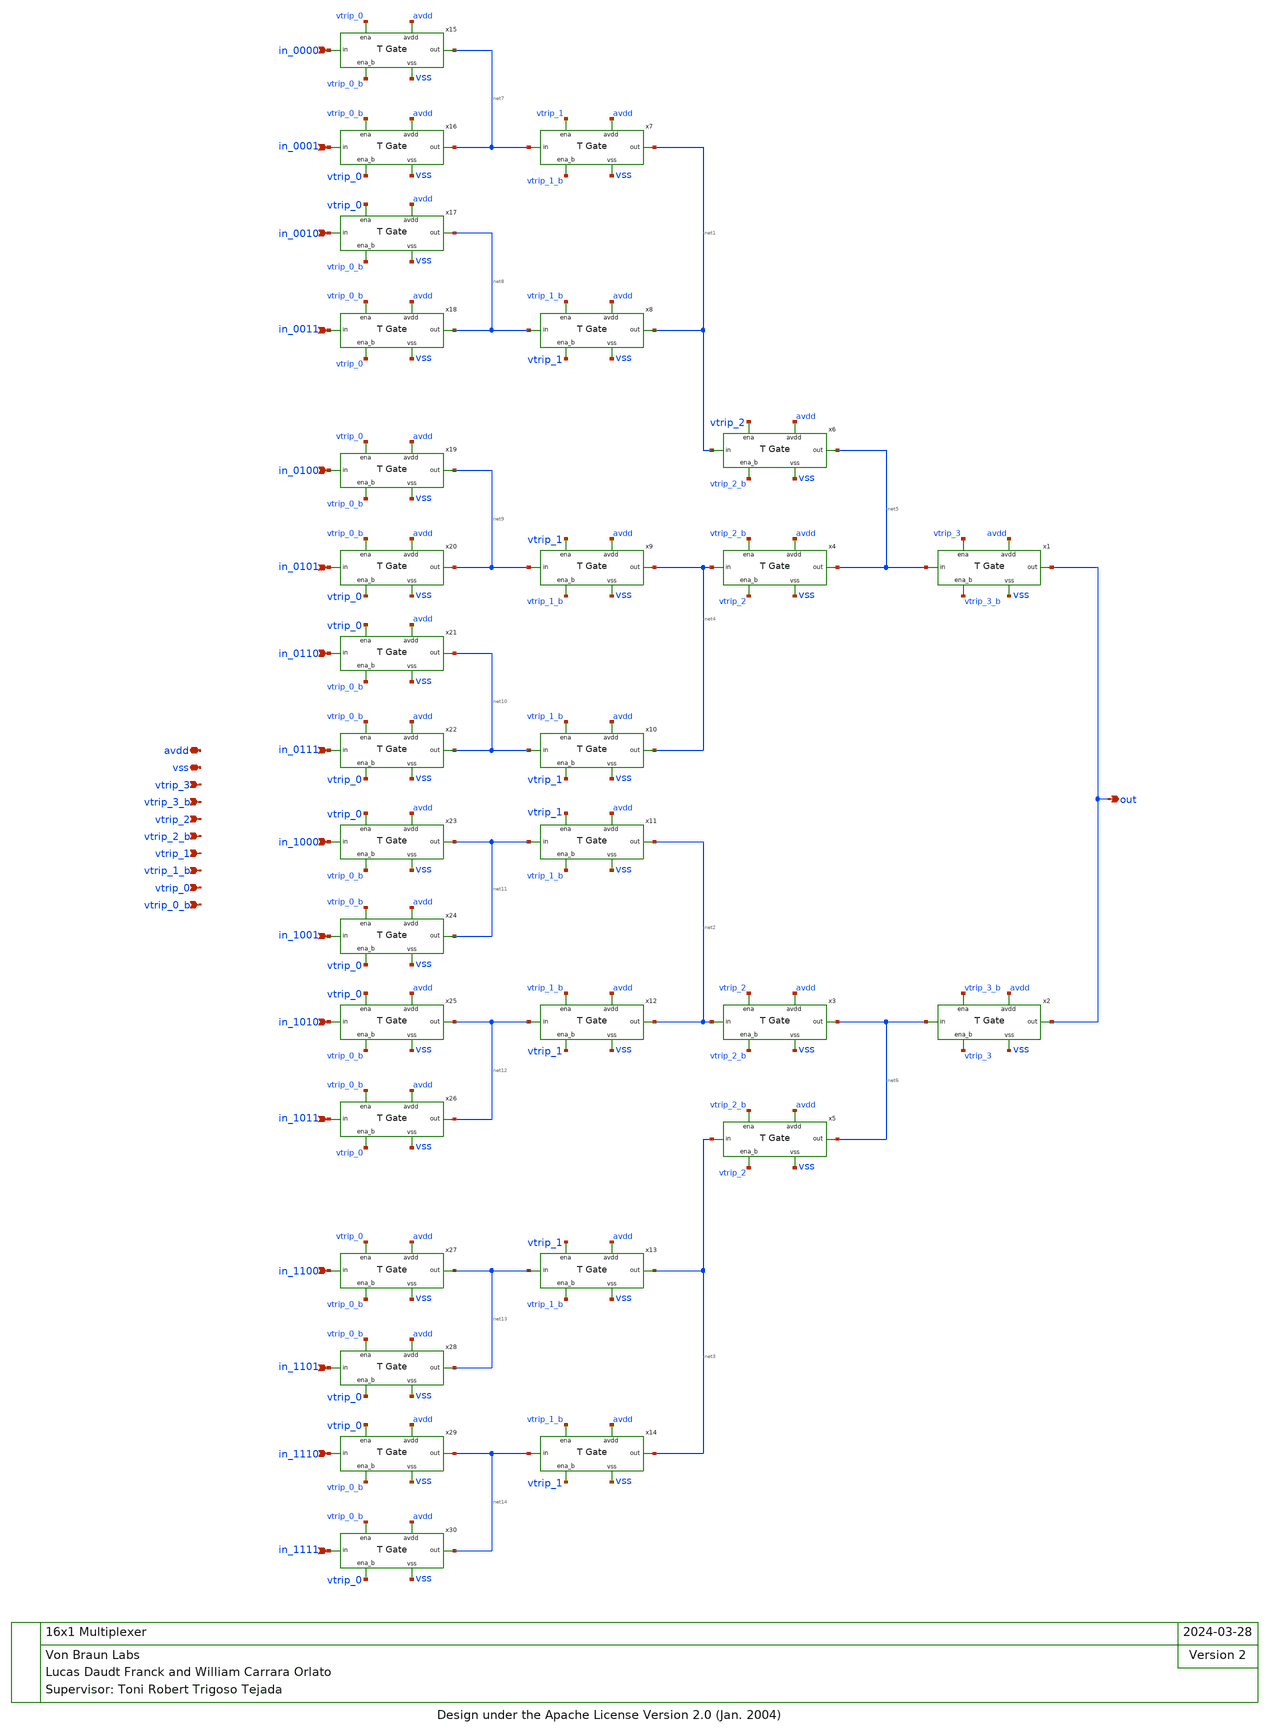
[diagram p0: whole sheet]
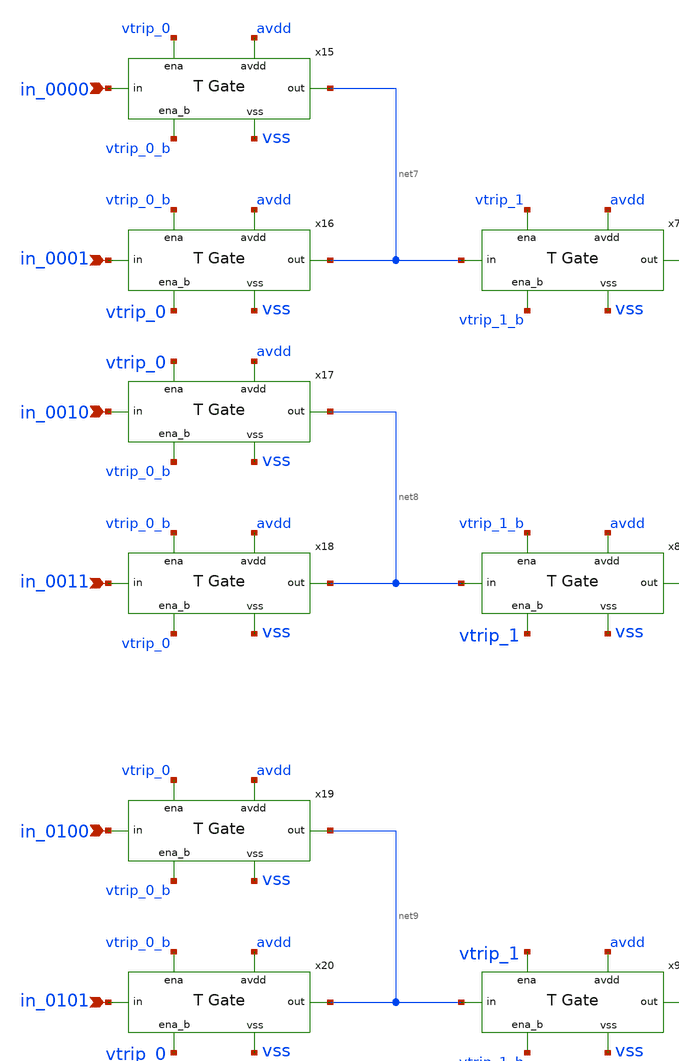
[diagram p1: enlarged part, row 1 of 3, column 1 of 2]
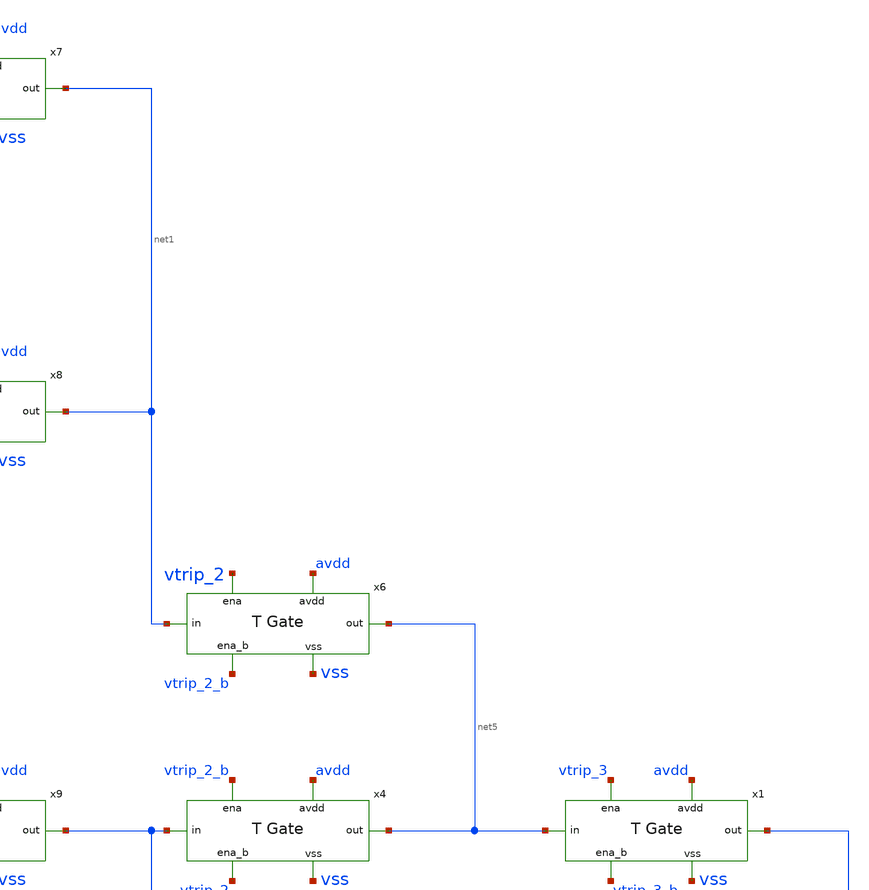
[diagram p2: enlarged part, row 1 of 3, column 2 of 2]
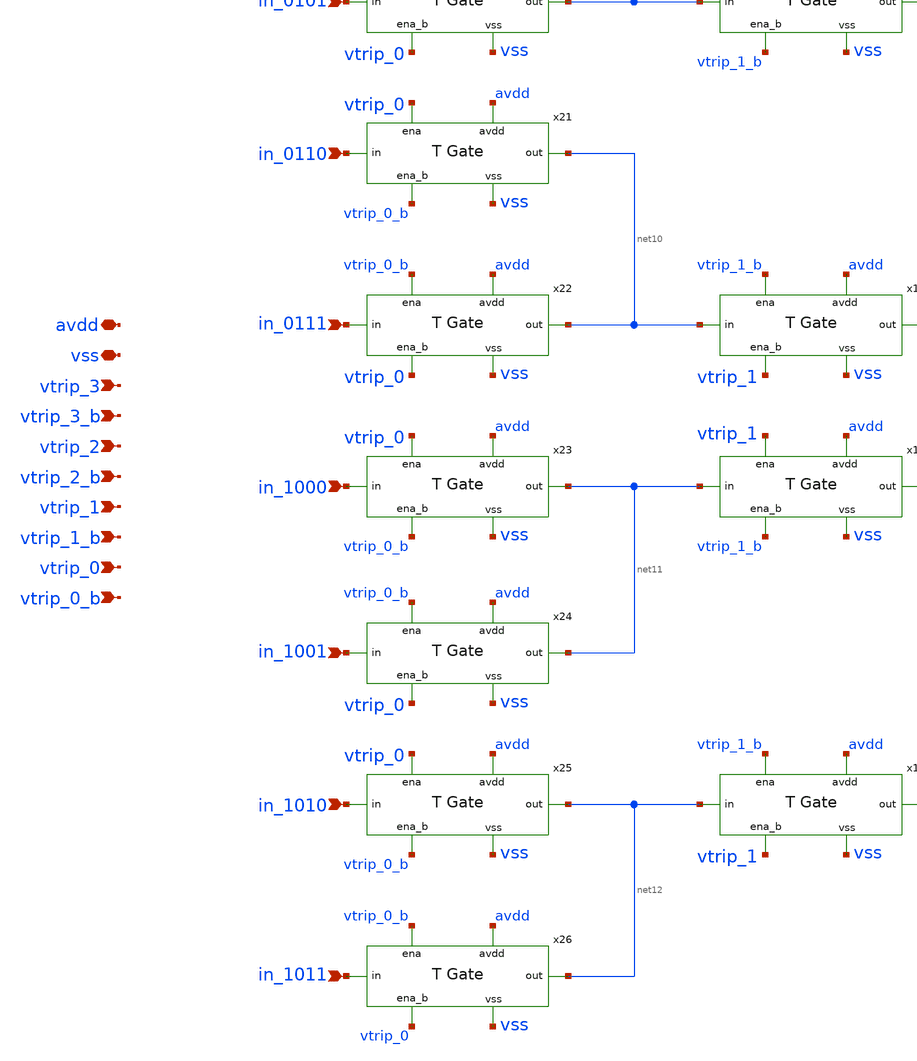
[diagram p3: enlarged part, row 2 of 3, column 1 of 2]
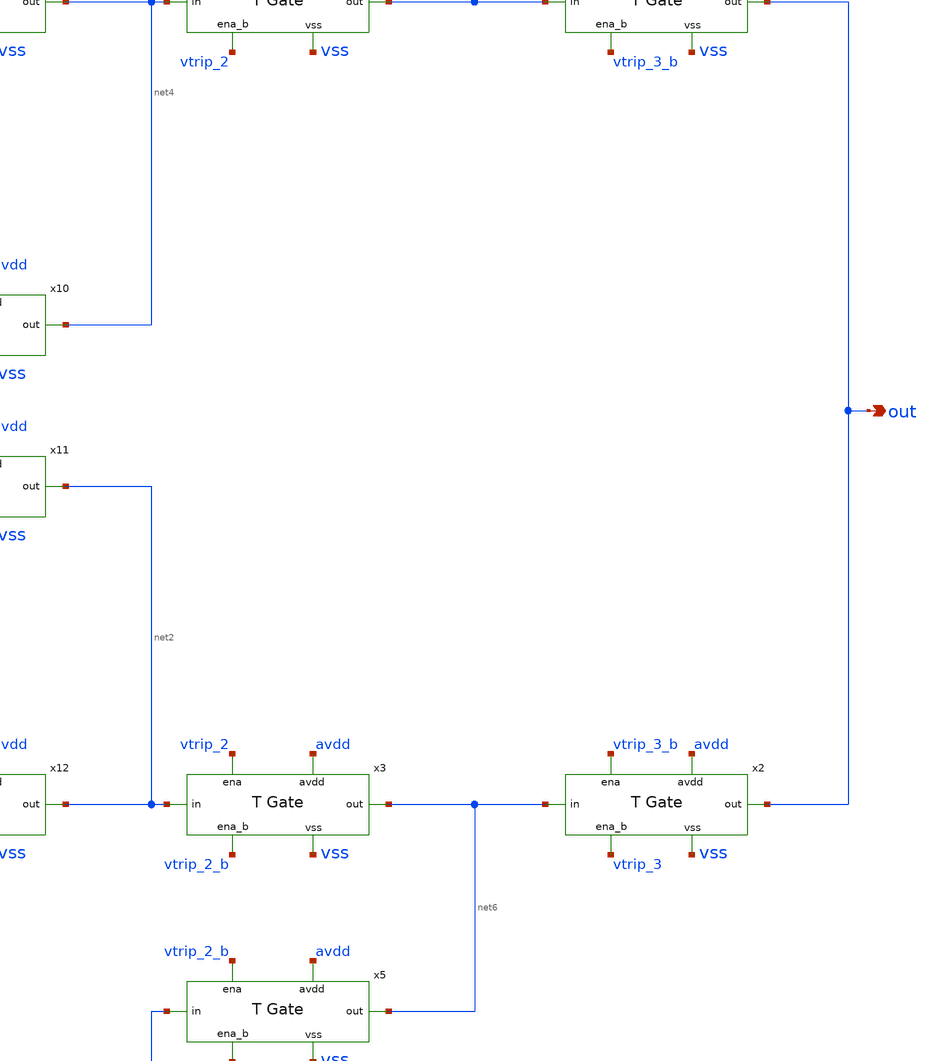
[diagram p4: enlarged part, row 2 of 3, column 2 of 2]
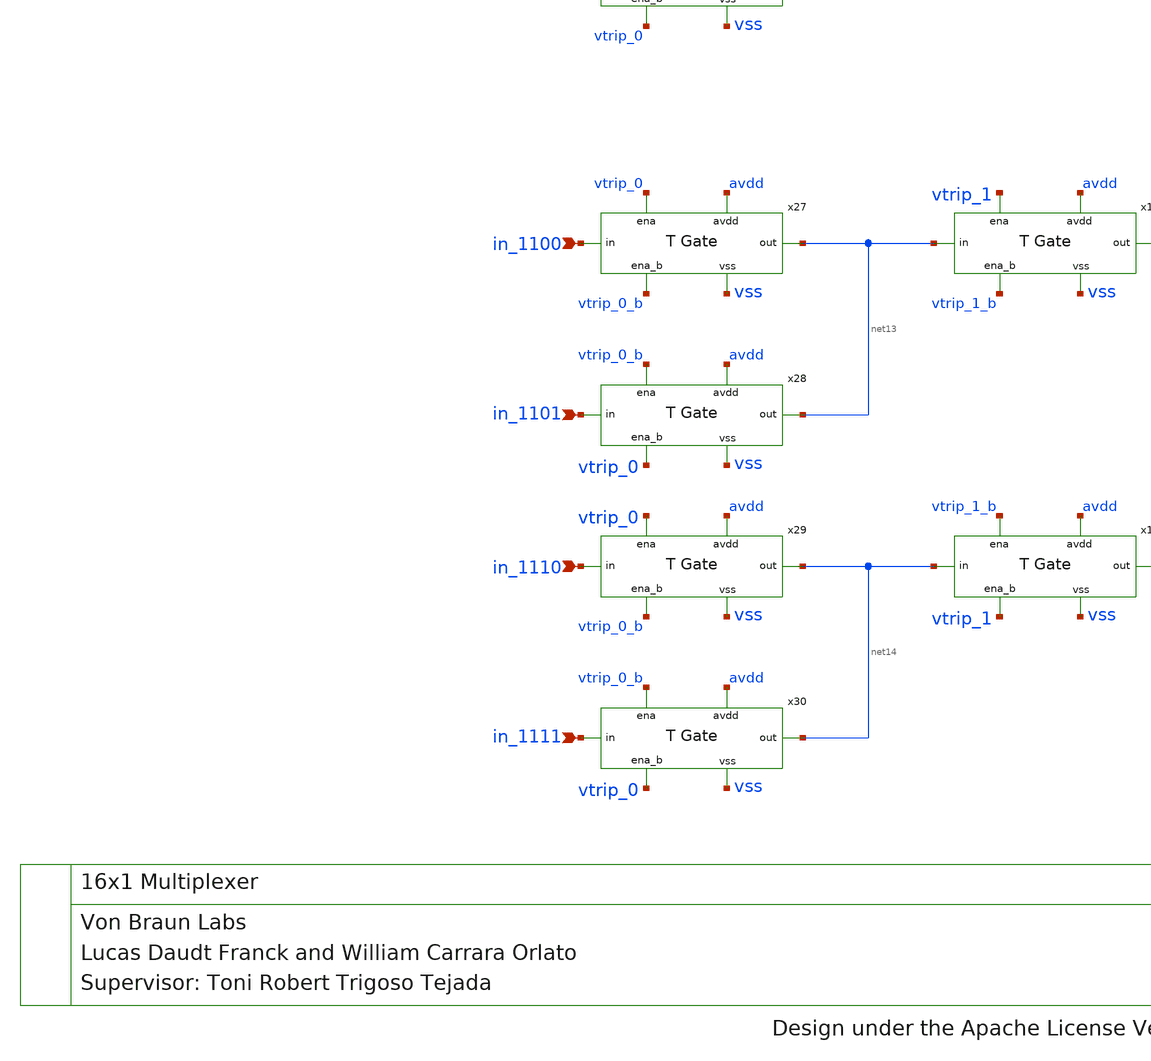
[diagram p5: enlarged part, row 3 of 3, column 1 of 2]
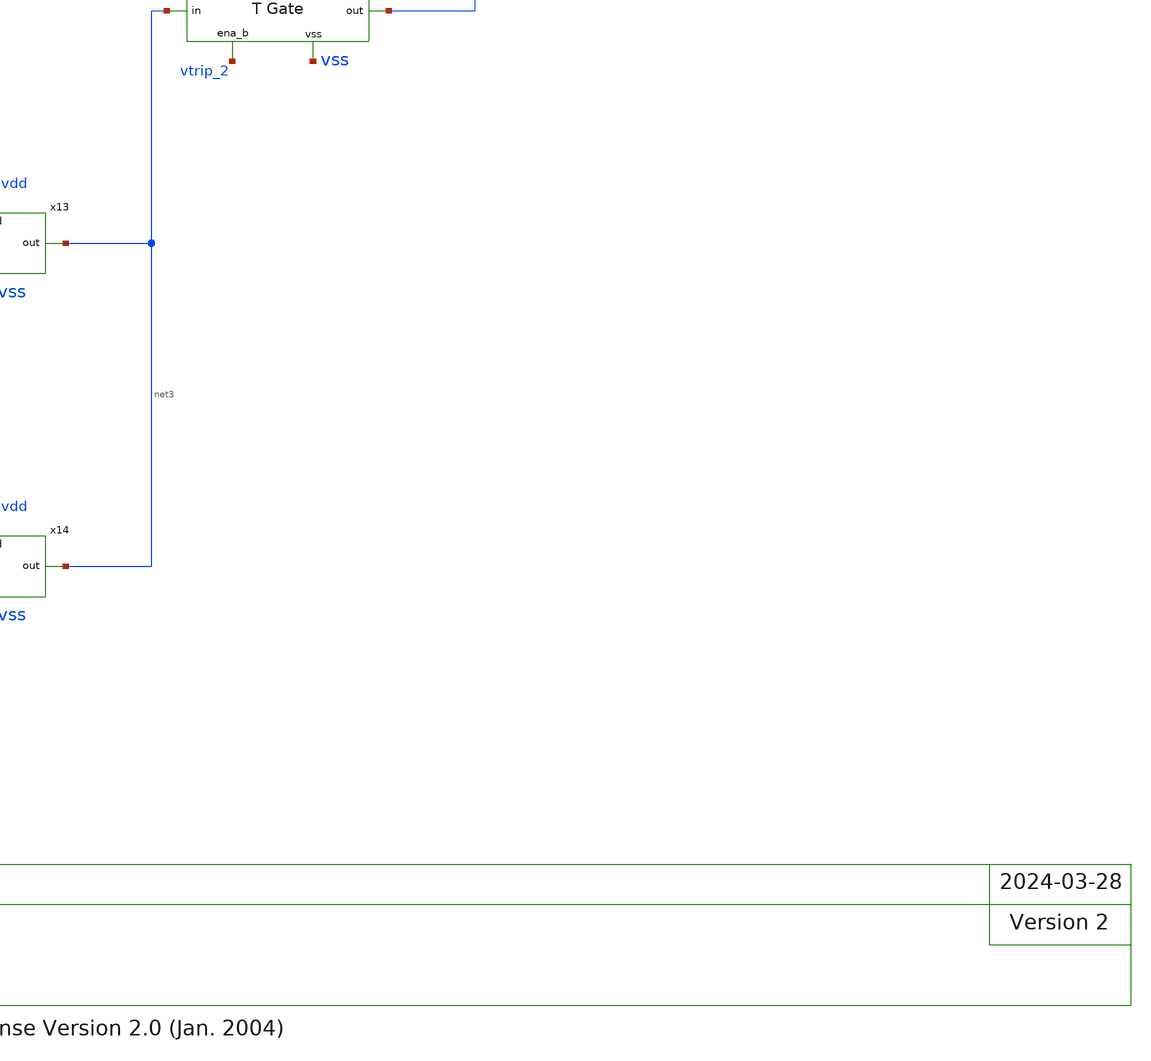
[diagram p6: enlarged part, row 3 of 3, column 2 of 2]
** sch_path: blocks/input/xschem/multiplexer.sch
* Design under the Apache License Version 2.0 (Jan. 2004)
**.subckt multiplexer in_0000 in_0001 in_0010 in_0011 in_0100 in_0101 in_0110 in_0111 in_1000
*+ in_1001 in_1010 in_1011 in_1110 in_1111 in_1100 in_1101 out vtrip_3 vtrip_3_b vtrip_2 vtrip_2_b vtrip_1
*+ vtrip_1_b vtrip_0 vtrip_0_b avdd vss
*.ipin in_0000
*.ipin in_0001
*.ipin in_0010
*.ipin in_0011
*.ipin in_0100
*.ipin in_0101
*.ipin in_0110
*.ipin in_0111
*.ipin in_1000
*.ipin in_1001
*.ipin in_1010
*.ipin in_1011
*.ipin in_1110
*.ipin in_1111
*.ipin in_1100
*.ipin in_1101
*.opin out
*.ipin vtrip_3
*.ipin vtrip_3_b
*.ipin vtrip_2
*.ipin vtrip_2_b
*.ipin vtrip_1
*.ipin vtrip_1_b
*.ipin vtrip_0
*.ipin vtrip_0_b
*.iopin avdd
*.iopin vss
x1 net5 vtrip_3_b vtrip_3 avdd vss out trans_gate
x2 net6 vtrip_3 vtrip_3_b avdd vss out trans_gate
x3 net2 vtrip_2_b vtrip_2 avdd vss net6 trans_gate
x4 net4 vtrip_2 vtrip_2_b avdd vss net5 trans_gate
x5 net3 vtrip_2 vtrip_2_b avdd vss net6 trans_gate
x6 net1 vtrip_2_b vtrip_2 avdd vss net5 trans_gate
x7 net7 vtrip_1_b vtrip_1 avdd vss net1 trans_gate
x8 net8 vtrip_1 vtrip_1_b avdd vss net1 trans_gate
x9 net9 vtrip_1_b vtrip_1 avdd vss net4 trans_gate
x10 net10 vtrip_1 vtrip_1_b avdd vss net4 trans_gate
x11 net11 vtrip_1_b vtrip_1 avdd vss net2 trans_gate
x12 net12 vtrip_1 vtrip_1_b avdd vss net2 trans_gate
x13 net13 vtrip_1_b vtrip_1 avdd vss net3 trans_gate
x14 net14 vtrip_1 vtrip_1_b avdd vss net3 trans_gate
x15 in_0000 vtrip_0_b vtrip_0 avdd vss net7 trans_gate
x16 in_0001 vtrip_0 vtrip_0_b avdd vss net7 trans_gate
x17 in_0010 vtrip_0_b vtrip_0 avdd vss net8 trans_gate
x18 in_0011 vtrip_0 vtrip_0_b avdd vss net8 trans_gate
x19 in_0100 vtrip_0_b vtrip_0 avdd vss net9 trans_gate
x20 in_0101 vtrip_0 vtrip_0_b avdd vss net9 trans_gate
x21 in_0110 vtrip_0_b vtrip_0 avdd vss net10 trans_gate
x22 in_0111 vtrip_0 vtrip_0_b avdd vss net10 trans_gate
x23 in_1000 vtrip_0_b vtrip_0 avdd vss net11 trans_gate
x24 in_1001 vtrip_0 vtrip_0_b avdd vss net11 trans_gate
x25 in_1010 vtrip_0_b vtrip_0 avdd vss net12 trans_gate
x26 in_1011 vtrip_0 vtrip_0_b avdd vss net12 trans_gate
x27 in_1100 vtrip_0_b vtrip_0 avdd vss net13 trans_gate
x28 in_1101 vtrip_0 vtrip_0_b avdd vss net13 trans_gate
x29 in_1110 vtrip_0_b vtrip_0 avdd vss net14 trans_gate
x30 in_1111 vtrip_0 vtrip_0_b avdd vss net14 trans_gate
**.ends

* expanding   symbol:  trans_gate.sym # of pins=6
** sym_path: blocks/comp_hyst/xschem/trans_gate.sym
** sch_path: blocks/comp_hyst/xschem/trans_gate.sch
.subckt trans_gate in ena_b ena avdd vss out
*.iopin avdd
*.iopin vss
*.ipin ena
*.ipin ena_b
*.ipin in
*.ipin out
XM1 in ena_b out vss sky130_fd_pr__nfet_g5v0d10v5 L=5 W=1 nf=1 ad='int((nf+1)/2) * W/nf * 0.29' as='int((nf+2)/2) * W/nf * 0.29'
+ pd='2*int((nf+1)/2) * (W/nf + 0.29)' ps='2*int((nf+2)/2) * (W/nf + 0.29)' nrd='0.29 / W' nrs='0.29 / W'
+ sa=0 sb=0 sd=0 mult=1 m=1
XM2 in ena out avdd sky130_fd_pr__pfet_g5v0d10v5 L=5 W=6 nf=1 ad='int((nf+1)/2) * W/nf * 0.29' as='int((nf+2)/2) * W/nf * 0.29'
+ pd='2*int((nf+1)/2) * (W/nf + 0.29)' ps='2*int((nf+2)/2) * (W/nf + 0.29)' nrd='0.29 / W' nrs='0.29 / W'
+ sa=0 sb=0 sd=0 mult=1 m=1
.ends

.end
